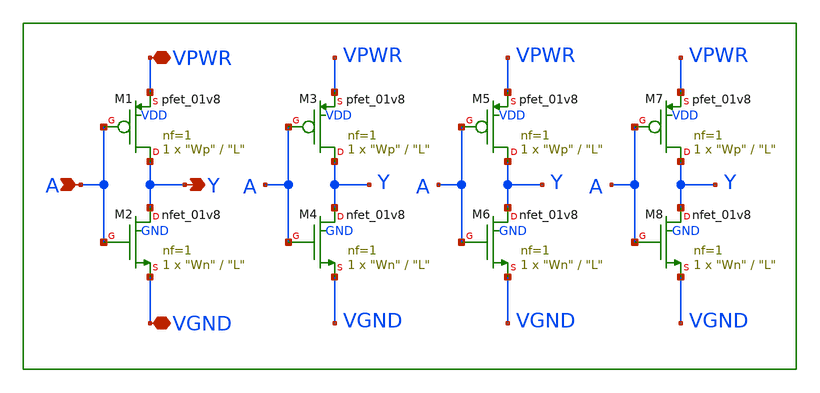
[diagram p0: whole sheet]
** sch_path: xschem/lib/main_inv.sch
**.subckt main_inv VPWR VGND A Y
*.iopin VPWR
*.iopin VGND
*.ipin A
*.opin Y
XM1 Y A VPWR VDD sky130_fd_pr__pfet_01v8 L="L" W="Wp" nf=1 ad='int((1 + 1)/2) * "Wp" / 1 * 0.29' as='int((1 + 2)/2) * "Wp" / 1 * 0.29'
+ pd='2*int((1 + 1)/2) * ("Wp" / 1 + 0.29)' ps='2*int((1 + 2)/2) * ("Wp" / 1 + 0.29)' nrd='0.29 / "Wp" '
+ nrs='0.29 / "Wp" ' sa=0 sb=0 sd=0 mult=1 m=1
XM2 Y A VGND GND sky130_fd_pr__nfet_01v8 L="L" W="Wn" nf=1 ad='int((nf+1)/2) * W/nf * 0.29' as='int((nf+2)/2) * W/nf * 0.29'
+ pd='2*int((nf+1)/2) * (W/nf + 0.29)' ps='2*int((nf+2)/2) * (W/nf + 0.29)' nrd='0.29 / W' nrs='0.29 / W'
+ sa=0 sb=0 sd=0 mult=1 m=1
XM3 Y A VPWR VDD sky130_fd_pr__pfet_01v8 L="L" W="Wp" nf=1 ad='int((1 + 1)/2) * "Wp" / 1 * 0.29' as='int((1 + 2)/2) * "Wp" / 1 * 0.29'
+ pd='2*int((1 + 1)/2) * ("Wp" / 1 + 0.29)' ps='2*int((1 + 2)/2) * ("Wp" / 1 + 0.29)' nrd='0.29 / "Wp" '
+ nrs='0.29 / "Wp" ' sa=0 sb=0 sd=0 mult=1 m=1
XM4 Y A VGND GND sky130_fd_pr__nfet_01v8 L="L" W="Wn" nf=1 ad='int((nf+1)/2) * W/nf * 0.29' as='int((nf+2)/2) * W/nf * 0.29'
+ pd='2*int((nf+1)/2) * (W/nf + 0.29)' ps='2*int((nf+2)/2) * (W/nf + 0.29)' nrd='0.29 / W' nrs='0.29 / W'
+ sa=0 sb=0 sd=0 mult=1 m=1
XM5 Y A VPWR VDD sky130_fd_pr__pfet_01v8 L="L" W="Wp" nf=1 ad='int((1 + 1)/2) * "Wp" / 1 * 0.29' as='int((1 + 2)/2) * "Wp" / 1 * 0.29'
+ pd='2*int((1 + 1)/2) * ("Wp" / 1 + 0.29)' ps='2*int((1 + 2)/2) * ("Wp" / 1 + 0.29)' nrd='0.29 / "Wp" '
+ nrs='0.29 / "Wp" ' sa=0 sb=0 sd=0 mult=1 m=1
XM6 Y A VGND GND sky130_fd_pr__nfet_01v8 L="L" W="Wn" nf=1 ad='int((nf+1)/2) * W/nf * 0.29' as='int((nf+2)/2) * W/nf * 0.29'
+ pd='2*int((nf+1)/2) * (W/nf + 0.29)' ps='2*int((nf+2)/2) * (W/nf + 0.29)' nrd='0.29 / W' nrs='0.29 / W'
+ sa=0 sb=0 sd=0 mult=1 m=1
XM7 Y A VPWR VDD sky130_fd_pr__pfet_01v8 L="L" W="Wp" nf=1 ad='int((1 + 1)/2) * "Wp" / 1 * 0.29' as='int((1 + 2)/2) * "Wp" / 1 * 0.29'
+ pd='2*int((1 + 1)/2) * ("Wp" / 1 + 0.29)' ps='2*int((1 + 2)/2) * ("Wp" / 1 + 0.29)' nrd='0.29 / "Wp" '
+ nrs='0.29 / "Wp" ' sa=0 sb=0 sd=0 mult=1 m=1
XM8 Y A VGND GND sky130_fd_pr__nfet_01v8 L="L" W="Wn" nf=1 ad='int((nf+1)/2) * W/nf * 0.29' as='int((nf+2)/2) * W/nf * 0.29'
+ pd='2*int((nf+1)/2) * (W/nf + 0.29)' ps='2*int((nf+2)/2) * (W/nf + 0.29)' nrd='0.29 / W' nrs='0.29 / W'
+ sa=0 sb=0 sd=0 mult=1 m=1
**.ends
.end
